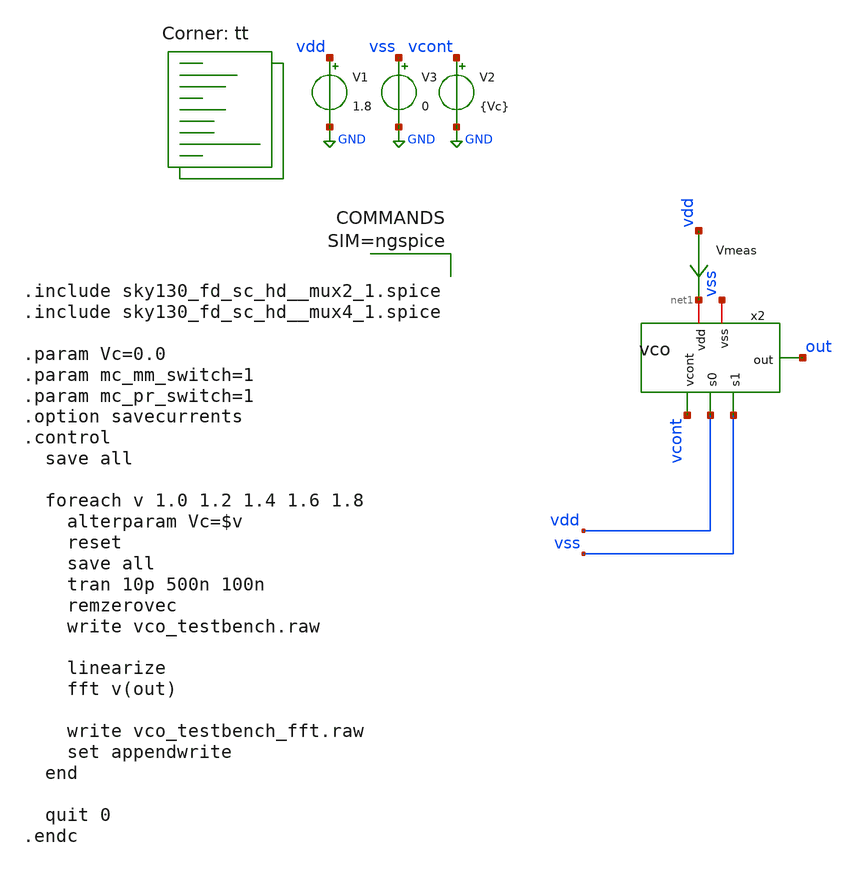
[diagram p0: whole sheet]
** sch_path: xschem/vco_testbench.sch
**.subckt vco_testbench
V1 vdd GND 1.8
V2 vcont GND {Vc}
x2 net1 vcont vdd vss out vss vco
V3 vss GND 0
Vmeas vdd net1 0
.save i(vmeas)
**** begin user architecture code
.lib $::SKYWATER_MODELS/sky130.lib.spice tt



.include sky130_fd_sc_hd__mux2_1.spice
.include sky130_fd_sc_hd__mux4_1.spice

.param Vc=0.0
.param mc_mm_switch=1
.param mc_pr_switch=1
.option savecurrents
.control
  save all

  foreach v 1.0 1.2 1.4 1.6 1.8
    alterparam Vc=$v
    reset
    save all
    tran 10p 500n 100n
    remzerovec
    write vco_testbench.raw

    linearize
    fft v(out)

    write vco_testbench_fft.raw
    set appendwrite
  end

  quit 0
.endc



**** end user architecture code
**.ends

* expanding   symbol:  vco.sym # of pins=6
** sym_path: xschem/vco.sym
** sch_path: xschem/vco.sch
.subckt vco vdd vcont s0 s1 out vss
*.iopin vdd
*.ipin s0
*.ipin s1
*.ipin vcont
*.iopin vss
*.opin out
x1 vdd vcont_b s0 s1 net2 net1 vcont vss delay_stage
x2 vdd vcont_b s0 s1 net3 net2 vcont vss delay_stage
x3 vdd vcont_b s0 s1 net4 net3 vcont vss delay_stage
C1 net2 0 10f m=1
C2 net3 0 10f m=1
C3 net4 0 10f m=1
XM5 vcont_b vcont_b vdd vdd sky130_fd_pr__pfet_01v8 L=0.15 W=2 nf=1 ad='int((nf+1)/2) * W/nf * 0.29'
+ as='int((nf+2)/2) * W/nf * 0.29' pd='2*int((nf+1)/2) * (W/nf + 0.29)' ps='2*int((nf+2)/2) * (W/nf + 0.29)'
+ nrd='0.29 / W' nrs='0.29 / W' sa=0 sb=0 sd=0 mult=1 m=1
XM6 vcont_b vcont vss vss sky130_fd_pr__nfet_01v8 L=0.15 W=1 nf=1 ad='int((nf+1)/2) * W/nf * 0.29' as='int((nf+2)/2) * W/nf * 0.29'
+ pd='2*int((nf+1)/2) * (W/nf + 0.29)' ps='2*int((nf+2)/2) * (W/nf + 0.29)' nrd='0.29 / W' nrs='0.29 / W'
+ sa=0 sb=0 sd=0 mult=1 m=1
x4 vdd vcont_b s0 s1 net5 net4 vcont vss delay_stage
C4 net5 0 10f m=1
x5 vdd vcont_b s0 s1 net6 net5 vcont vss delay_stage
C5 net6 0 10f m=1
x6 vdd vcont_b s0 s1 net7 net6 vcont vss delay_stage
C6 net7 0 10f m=1
x7 vdd vcont_b s0 s1 net8 net7 vcont vss delay_stage
C7 net8 0 10f m=1
x9 vdd vcont_b s0 s1 net9 net8 vcont vss delay_stage
C8 net9 0 10f m=1
x10 vdd vcont_b s0 s1 net10 net9 vcont vss delay_stage
C9 net10 0 10f m=1
x11 net22 net14 net8 net4 s1 s0 vss vss vdd vdd net1 sky130_fd_sc_hd__mux4_1
x8 vdd vcont_b s0 s1 net11 net10 vcont vss delay_stage
x12 vdd vcont_b s0 s1 net12 net11 vcont vss delay_stage
x13 vdd vcont_b s0 s1 net13 net12 vcont vss delay_stage
C10 net11 0 10f m=1
C11 net12 0 10f m=1
C12 net13 0 10f m=1
x14 vdd vcont_b s0 s1 net14 net13 vcont vss delay_stage
C13 net14 0 10f m=1
x15 vdd vcont_b s0 s1 net15 net14 vcont vss delay_stage
C14 net15 0 10f m=1
x16 vdd vcont_b s0 s1 net16 net15 vcont vss delay_stage
C15 net16 0 10f m=1
x17 vdd vcont_b s0 s1 net17 net16 vcont vss delay_stage
C16 net17 0 10f m=1
x18 vdd vcont_b s0 s1 net18 net17 vcont vss delay_stage
C17 net18 0 10f m=1
x19 vdd vcont_b s0 s1 net19 net18 vcont vss delay_stage
C18 net19 0 10f m=1
x20 vdd vcont_b s0 s1 net20 net19 vcont vss delay_stage
C19 net20 0 10f m=1
x21 vdd vcont_b s0 s1 net21 net20 vcont vss delay_stage
C20 net21 0 10f m=1
x22 vdd vcont_b s0 s1 net22 net21 vcont vss delay_stage
C21 net22 0 10f m=1
XM3 out net1 vss vss sky130_fd_pr__nfet_01v8 L=0.15 W=1 nf=1 ad='int((1 + 1)/2) * 1 / 1 * 0.29' as='int((1 + 2)/2) * 1 / 1 * 0.29'
+ pd='2*int((1 + 1)/2) * (1 / 1 + 0.29)' ps='2*int((1 + 2)/2) * (1 / 1 + 0.29)' nrd='0.29 / 1 ' nrs='0.29 / 1 '
+ sa=0 sb=0 sd=0 mult=1 m=1
XM4 out net1 vdd vdd sky130_fd_pr__pfet_01v8 L=0.15 W=2 nf=1 ad='int((nf+1)/2) * W/nf * 0.29' as='int((nf+2)/2) * W/nf * 0.29'
+ pd='2*int((nf+1)/2) * (W/nf + 0.29)' ps='2*int((nf+2)/2) * (W/nf + 0.29)' nrd='0.29 / W' nrs='0.29 / W'
+ sa=0 sb=0 sd=0 mult=1 m=1
.ends


* expanding   symbol:  delay_stage.sym # of pins=8
** sym_path: xschem/delay_stage.sym
** sch_path: xschem/delay_stage.sch
.subckt delay_stage vdd vcont_p s0 s1 out in vcont_n vss
*.ipin in
*.opin out
*.iopin vdd
*.ipin vcont_n
*.ipin vcont_p
*.ipin s0
*.ipin s1
*.iopin vss
XM3 out in net2 vss sky130_fd_pr__nfet_01v8 L=0.15 W=1 nf=1 ad='int((nf+1)/2) * W/nf * 0.29' as='int((nf+2)/2) * W/nf * 0.29'
+ pd='2*int((nf+1)/2) * (W/nf + 0.29)' ps='2*int((nf+2)/2) * (W/nf + 0.29)' nrd='0.29 / W' nrs='0.29 / W'
+ sa=0 sb=0 sd=0 mult=1 m=1
XM2 out in net1 vdd sky130_fd_pr__pfet_01v8 L=0.15 W=2 nf=1 ad='int((nf+1)/2) * W/nf * 0.29' as='int((nf+2)/2) * W/nf * 0.29'
+ pd='2*int((nf+1)/2) * (W/nf + 0.29)' ps='2*int((nf+2)/2) * (W/nf + 0.29)' nrd='0.29 / W' nrs='0.29 / W'
+ sa=0 sb=0 sd=0 mult=1 m=1
XM1 net1 vcont_p vdd vdd sky130_fd_pr__pfet_01v8 L=0.15 W=2 nf=1 ad='int((nf+1)/2) * W/nf * 0.29' as='int((nf+2)/2) * W/nf * 0.29'
+ pd='2*int((nf+1)/2) * (W/nf + 0.29)' ps='2*int((nf+2)/2) * (W/nf + 0.29)' nrd='0.29 / W' nrs='0.29 / W'
+ sa=0 sb=0 sd=0 mult=1 m=1
XM4 net2 vcont_n vss vss sky130_fd_pr__nfet_01v8 L=0.15 W=1 nf=1 ad='int((nf+1)/2) * W/nf * 0.29' as='int((nf+2)/2) * W/nf * 0.29'
+ pd='2*int((nf+1)/2) * (W/nf + 0.29)' ps='2*int((nf+2)/2) * (W/nf + 0.29)' nrd='0.29 / W' nrs='0.29 / W'
+ sa=0 sb=0 sd=0 mult=1 m=1
XC2 net3 vss sky130_fd_pr__cap_mim_m3_1 W=2.1 L=2.1 MF=1 m=1
XC1 net4 vss sky130_fd_pr__cap_mim_m3_1 W=2.1 L=4.2 MF=1 m=1
XM5 out s0 net4 vss sky130_fd_pr__nfet_01v8 L=0.15 W=1 nf=1 ad='int((nf+1)/2) * W/nf * 0.29' as='int((nf+2)/2) * W/nf * 0.29'
+ pd='2*int((nf+1)/2) * (W/nf + 0.29)' ps='2*int((nf+2)/2) * (W/nf + 0.29)' nrd='0.29 / W' nrs='0.29 / W'
+ sa=0 sb=0 sd=0 mult=1 m=1
XM6 out s1 net3 vss sky130_fd_pr__nfet_01v8 L=0.15 W=1 nf=1 ad='int((nf+1)/2) * W/nf * 0.29' as='int((nf+2)/2) * W/nf * 0.29'
+ pd='2*int((nf+1)/2) * (W/nf + 0.29)' ps='2*int((nf+2)/2) * (W/nf + 0.29)' nrd='0.29 / W' nrs='0.29 / W'
+ sa=0 sb=0 sd=0 mult=1 m=1
.ends

.GLOBAL GND
.end
